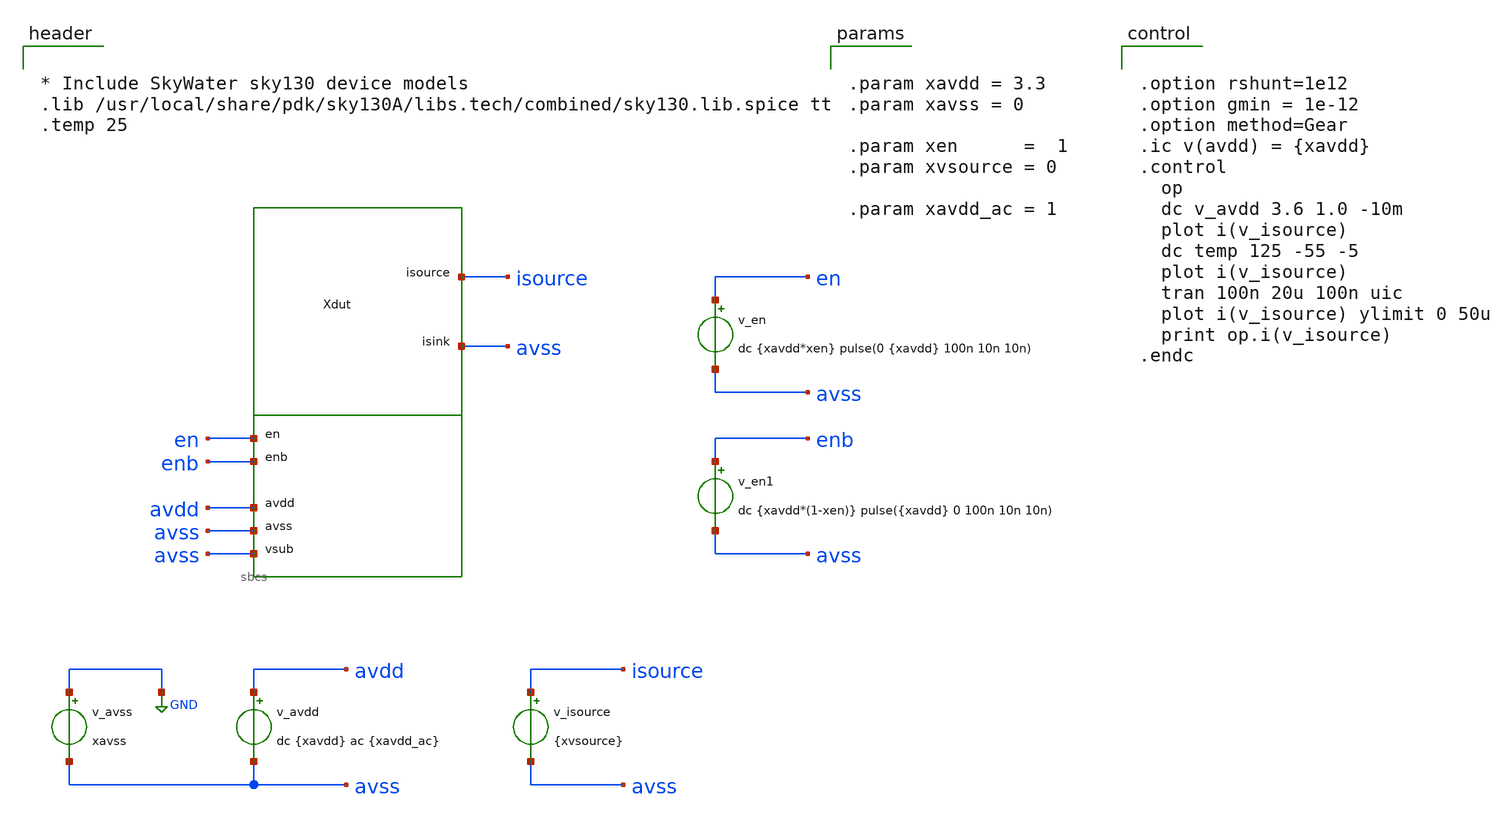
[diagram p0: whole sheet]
** sch_path: xschem/tb_sbcs.sch
**.subckt tb_sbcs
v_avss GND avss xavss
v_avdd avdd avss dc {xavdd} ac {xavdd_ac}
v_isource isource avss {xvsource}
Xdut isource avss en enb avdd avss avss sbcs
v_en en avss dc {xavdd*xen} pulse(0 {xavdd} 100n 10n 10n)
v_en1 enb avss dc {xavdd*(1-xen)} pulse({xavdd} 0 100n 10n 10n)
**** begin user architecture code


* Include SkyWater sky130 device models
.lib /usr/local/share/pdk/sky130A/libs.tech/combined/sky130.lib.spice tt
.temp 25




.option rshunt=1e12
.option gmin = 1e-12
.option method=Gear
.ic v(avdd) = {xavdd}
.control
  op
  dc v_avdd 3.6 1.0 -10m
  plot i(v_isource)
  dc temp 125 -55 -5
  plot i(v_isource)
  tran 100n 20u 100n uic
  plot i(v_isource) ylimit 0 50u
  print op.i(v_isource)
.endc




.param xavdd = 3.3
.param xavss = 0

.param xen      =  1
.param xvsource = 0

.param xavdd_ac = 1


**** end user architecture code
**.ends
.GLOBAL GND
.end
